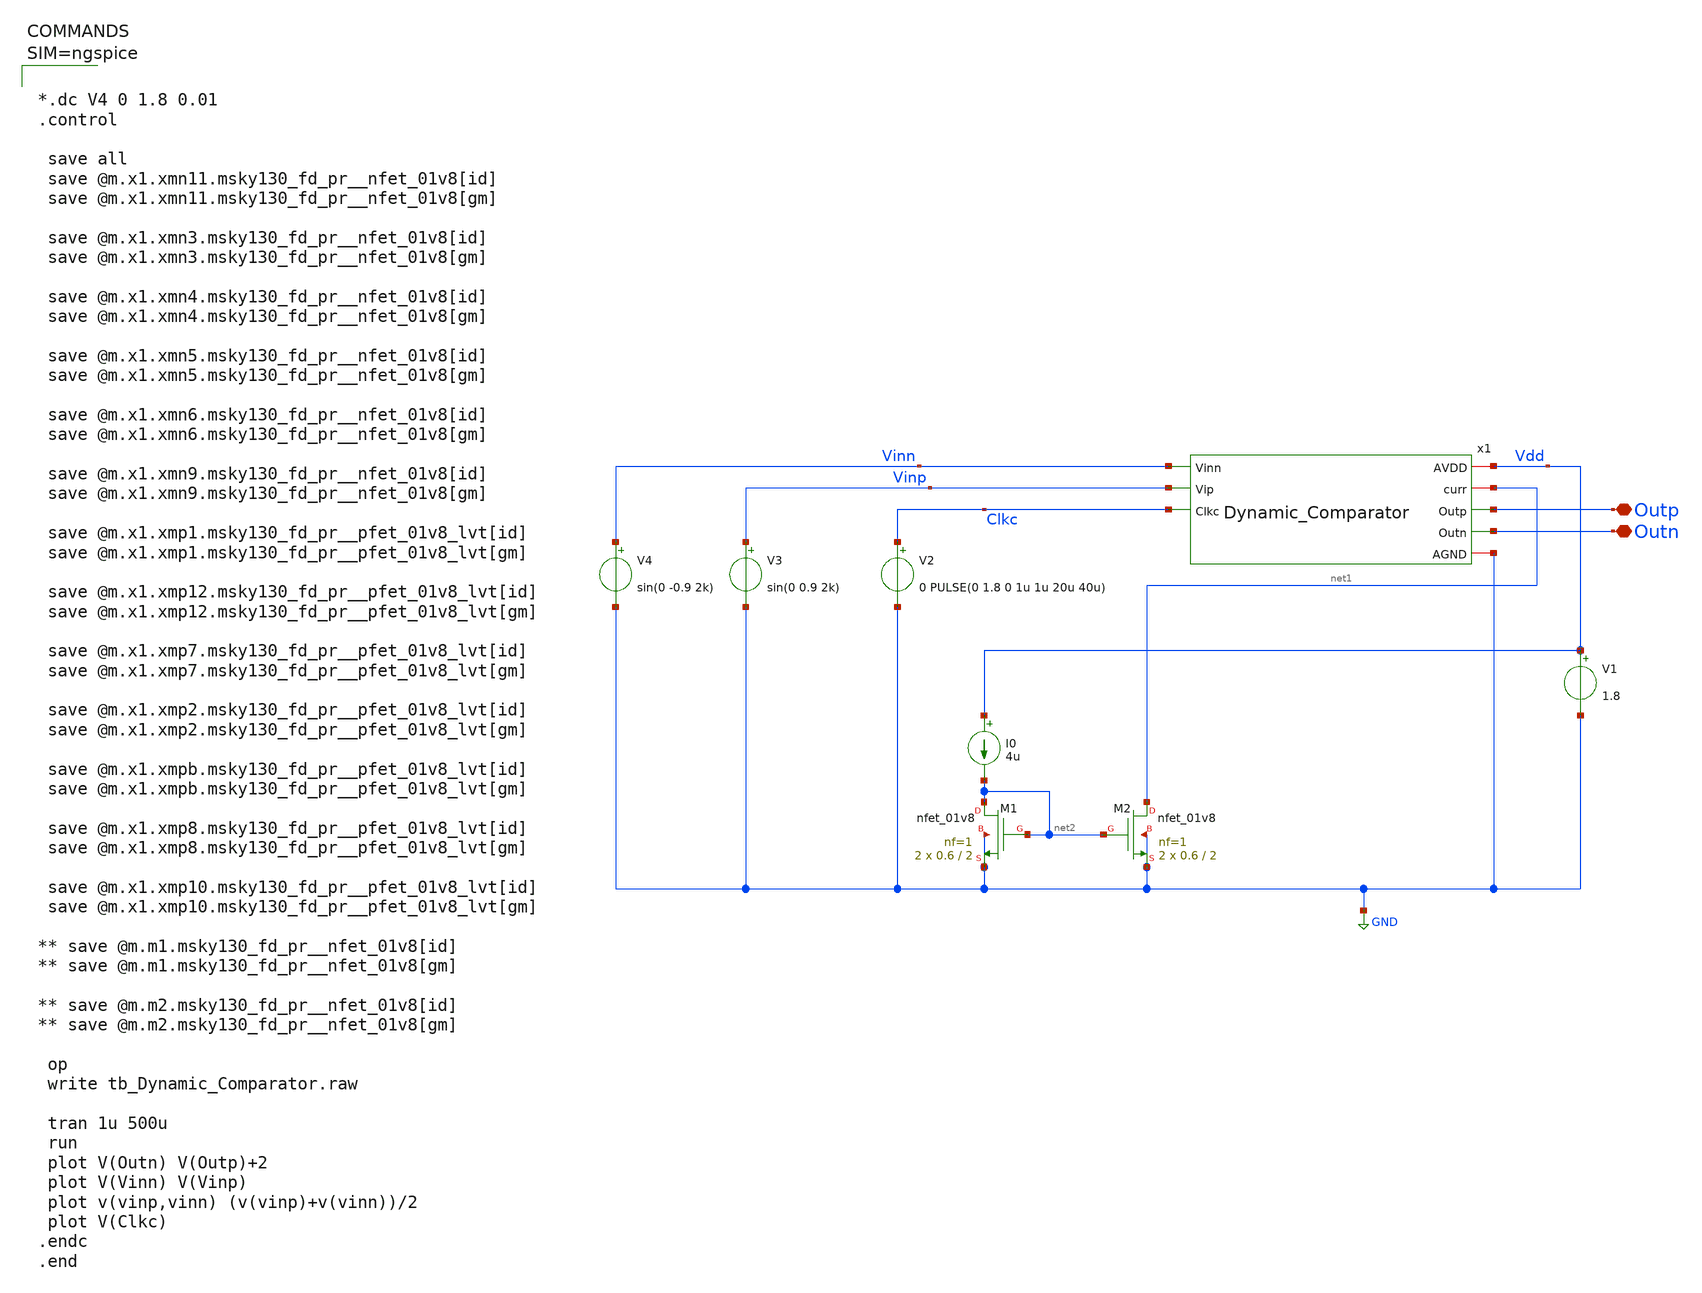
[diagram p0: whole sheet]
** sch_path: sar-adc/updated/tb_Dynamic_Comparator.sch
**.subckt tb_Dynamic_Comparator Outp Outn
*.iopin Outp
*.iopin Outn
V1 Vdd GND 1.8
V2 Clkc GND 0 PULSE(0 1.8 0 1u 1u 20u 40u)
V3 Vinp GND sin(0 0.9 2k)
V4 Vinn GND sin(0 -0.9 2k)
XM2 net1 net2 GND GND sky130_fd_pr__nfet_01v8 L=2 W=0.6 nf=1 ad='int((1 + 1)/2) * 0.6 / 1 * 0.29' as='int((1 + 2)/2) * 0.6 / 1 * 0.29'
+ pd='2*int((1 + 1)/2) * (0.6 / 1 + 0.29)' ps='2*int((1 + 2)/2) * (0.6 / 1 + 0.29)' nrd='0.29 / 0.6 ' nrs='0.29 / 0.6 '
+ sa=0 sb=0 sd=0 mult=2 m=2
XM1 net2 net2 GND GND sky130_fd_pr__nfet_01v8 L=2 W=0.6 nf=1 ad='int((1 + 1)/2) * 0.6 / 1 * 0.29' as='int((1 + 2)/2) * 0.6 / 1 * 0.29'
+ pd='2*int((1 + 1)/2) * (0.6 / 1 + 0.29)' ps='2*int((1 + 2)/2) * (0.6 / 1 + 0.29)' nrd='0.29 / 0.6 ' nrs='0.29 / 0.6 '
+ sa=0 sb=0 sd=0 mult=2 m=2
I0 Vdd net2 4u
x1 Vdd net1 Vinn Vinp Outp Outn Clkc GND Dynamic_Comparator
**** begin user architecture code

** opencircuitdesign pdks install
.lib $::SKYWATER_MODELS/sky130.lib.spice tt




*.dc V4 0 1.8 0.01
.control

 save all
 save @m.x1.xmn11.msky130_fd_pr__nfet_01v8[id]
 save @m.x1.xmn11.msky130_fd_pr__nfet_01v8[gm]

 save @m.x1.xmn3.msky130_fd_pr__nfet_01v8[id]
 save @m.x1.xmn3.msky130_fd_pr__nfet_01v8[gm]

 save @m.x1.xmn4.msky130_fd_pr__nfet_01v8[id]
 save @m.x1.xmn4.msky130_fd_pr__nfet_01v8[gm]

 save @m.x1.xmn5.msky130_fd_pr__nfet_01v8[id]
 save @m.x1.xmn5.msky130_fd_pr__nfet_01v8[gm]

 save @m.x1.xmn6.msky130_fd_pr__nfet_01v8[id]
 save @m.x1.xmn6.msky130_fd_pr__nfet_01v8[gm]

 save @m.x1.xmn9.msky130_fd_pr__nfet_01v8[id]
 save @m.x1.xmn9.msky130_fd_pr__nfet_01v8[gm]

 save @m.x1.xmp1.msky130_fd_pr__pfet_01v8_lvt[id]
 save @m.x1.xmp1.msky130_fd_pr__pfet_01v8_lvt[gm]

 save @m.x1.xmp12.msky130_fd_pr__pfet_01v8_lvt[id]
 save @m.x1.xmp12.msky130_fd_pr__pfet_01v8_lvt[gm]

 save @m.x1.xmp7.msky130_fd_pr__pfet_01v8_lvt[id]
 save @m.x1.xmp7.msky130_fd_pr__pfet_01v8_lvt[gm]

 save @m.x1.xmp2.msky130_fd_pr__pfet_01v8_lvt[id]
 save @m.x1.xmp2.msky130_fd_pr__pfet_01v8_lvt[gm]

 save @m.x1.xmpb.msky130_fd_pr__pfet_01v8_lvt[id]
 save @m.x1.xmpb.msky130_fd_pr__pfet_01v8_lvt[gm]

 save @m.x1.xmp8.msky130_fd_pr__pfet_01v8_lvt[id]
 save @m.x1.xmp8.msky130_fd_pr__pfet_01v8_lvt[gm]

 save @m.x1.xmp10.msky130_fd_pr__pfet_01v8_lvt[id]
 save @m.x1.xmp10.msky130_fd_pr__pfet_01v8_lvt[gm]

** save @m.m1.msky130_fd_pr__nfet_01v8[id]
** save @m.m1.msky130_fd_pr__nfet_01v8[gm]

** save @m.m2.msky130_fd_pr__nfet_01v8[id]
** save @m.m2.msky130_fd_pr__nfet_01v8[gm]

 op
 write tb_Dynamic_Comparator.raw

 tran 1u 500u
 run
 plot V(Outn) V(Outp)+2
 plot V(Vinn) V(Vinp)
 plot v(vinp,vinn) (v(vinp)+v(vinn))/2
 plot V(Clkc)
.endc
.end



**** end user architecture code
**.ends

* expanding   symbol:  Dynamic_Comparator.sym # of pins=8
** sym_path: sar-adc/updated/Dynamic_Comparator.sym
** sch_path: sar-adc/updated/Dynamic_Comparator.sch
.subckt Dynamic_Comparator AVDD curr Vinn Vip Outp Outn Clkc AGND
*.ipin Vip
*.ipin Vinn
*.opin Outn
*.opin Outp
*.ipin Clkc
*.iopin AVDD
*.iopin AGND
*.iopin curr
XMPB net1 curr AVDD AVDD sky130_fd_pr__pfet_01v8_lvt L=2 W=1.12 nf=1 ad='int((1 + 1)/2) * 1.12 / 1 * 0.29'
+ as='int((1 + 2)/2) * 1.12 / 1 * 0.29' pd='2*int((1 + 1)/2) * (1.12 / 1 + 0.29)' ps='2*int((1 + 2)/2) * (1.12 / 1 + 0.29)'
+ nrd='0.29 / 1.12 ' nrs='0.29 / 1.12 ' sa=0 sb=0 sd=0 mult=4 m=4
XMP7 net2 Clkc net1 AVDD sky130_fd_pr__pfet_01v8_lvt L=2 W=1.12 nf=1 ad='int((1 + 1)/2) * 1.12 / 1 * 0.29'
+ as='int((1 + 2)/2) * 1.12 / 1 * 0.29' pd='2*int((1 + 1)/2) * (1.12 / 1 + 0.29)' ps='2*int((1 + 2)/2) * (1.12 / 1 + 0.29)'
+ nrd='0.29 / 1.12 ' nrs='0.29 / 1.12 ' sa=0 sb=0 sd=0 mult=4 m=4
XMP12 curr curr AVDD AVDD sky130_fd_pr__pfet_01v8_lvt L=2 W=1.12 nf=1 ad='int((1 + 1)/2) * 1.12 / 1 * 0.29'
+ as='int((1 + 2)/2) * 1.12 / 1 * 0.29' pd='2*int((1 + 1)/2) * (1.12 / 1 + 0.29)' ps='2*int((1 + 2)/2) * (1.12 / 1 + 0.29)'
+ nrd='0.29 / 1.12 ' nrs='0.29 / 1.12 ' sa=0 sb=0 sd=0 mult=4 m=4
XMP1 net4 Vip net2 AVDD sky130_fd_pr__pfet_01v8_lvt L=2 W=2 nf=1 ad='int((1 + 1)/2) * 2 / 1 * 0.29' as='int((1 + 2)/2) * 2 / 1 * 0.29'
+ pd='2*int((1 + 1)/2) * (2 / 1 + 0.29)' ps='2*int((1 + 2)/2) * (2 / 1 + 0.29)' nrd='0.29 / 2 ' nrs='0.29 / 2 '
+ sa=0 sb=0 sd=0 mult=9 m=9
XMP2 net3 Vinn net2 AVDD sky130_fd_pr__pfet_01v8_lvt L=2 W=2 nf=1 ad='int((1 + 1)/2) * 2 / 1 * 0.29'
+ as='int((1 + 2)/2) * 2 / 1 * 0.29' pd='2*int((1 + 1)/2) * (2 / 1 + 0.29)' ps='2*int((1 + 2)/2) * (2 / 1 + 0.29)'
+ nrd='0.29 / 2 ' nrs='0.29 / 2 ' sa=0 sb=0 sd=0 mult=9 m=9
XMP8 Outp net4 AVDD AVDD sky130_fd_pr__pfet_01v8_lvt L=2 W=1.12 nf=1 ad='int((1 + 1)/2) * 1.12 / 1 * 0.29'
+ as='int((1 + 2)/2) * 1.12 / 1 * 0.29' pd='2*int((1 + 1)/2) * (1.12 / 1 + 0.29)' ps='2*int((1 + 2)/2) * (1.12 / 1 + 0.29)'
+ nrd='0.29 / 1.12 ' nrs='0.29 / 1.12 ' sa=0 sb=0 sd=0 mult=4 m=4
XMP10 Outn net3 AVDD AVDD sky130_fd_pr__pfet_01v8_lvt L=2 W=1.12 nf=1 ad='int((1 + 1)/2) * 1.12 / 1 * 0.29'
+ as='int((1 + 2)/2) * 1.12 / 1 * 0.29' pd='2*int((1 + 1)/2) * (1.12 / 1 + 0.29)' ps='2*int((1 + 2)/2) * (1.12 / 1 + 0.29)'
+ nrd='0.29 / 1.12 ' nrs='0.29 / 1.12 ' sa=0 sb=0 sd=0 mult=4 m=4
XMN5 net4 Clkc AGND AGND sky130_fd_pr__nfet_01v8 L=2 W=0.65 nf=1 ad='int((1 + 1)/2) * 0.65 / 1 * 0.29'
+ as='int((1 + 2)/2) * 0.65 / 1 * 0.29' pd='2*int((1 + 1)/2) * (0.65 / 1 + 0.29)' ps='2*int((1 + 2)/2) * (0.65 / 1 + 0.29)'
+ nrd='0.29 / 0.65 ' nrs='0.29 / 0.65 ' sa=0 sb=0 sd=0 mult=2 m=2
XMN3 net4 net3 AGND AGND sky130_fd_pr__nfet_01v8 L=2 W=0.6 nf=1 ad='int((1 + 1)/2) * 0.6 / 1 * 0.29'
+ as='int((1 + 2)/2) * 0.6 / 1 * 0.29' pd='2*int((1 + 1)/2) * (0.6 / 1 + 0.29)' ps='2*int((1 + 2)/2) * (0.6 / 1 + 0.29)'
+ nrd='0.29 / 0.6 ' nrs='0.29 / 0.6 ' sa=0 sb=0 sd=0 mult=2 m=2
XMN4 net3 net4 AGND AGND sky130_fd_pr__nfet_01v8 L=2 W=0.6 nf=1 ad='int((1 + 1)/2) * 0.6 / 1 * 0.29'
+ as='int((1 + 2)/2) * 0.6 / 1 * 0.29' pd='2*int((1 + 1)/2) * (0.6 / 1 + 0.29)' ps='2*int((1 + 2)/2) * (0.6 / 1 + 0.29)'
+ nrd='0.29 / 0.6 ' nrs='0.29 / 0.6 ' sa=0 sb=0 sd=0 mult=2 m=2
XMN6 net3 Clkc AGND AGND sky130_fd_pr__nfet_01v8 L=2 W=0.65 nf=1 ad='int((1 + 1)/2) * 0.65 / 1 * 0.29'
+ as='int((1 + 2)/2) * 0.65 / 1 * 0.29' pd='2*int((1 + 1)/2) * (0.65 / 1 + 0.29)' ps='2*int((1 + 2)/2) * (0.65 / 1 + 0.29)'
+ nrd='0.29 / 0.65 ' nrs='0.29 / 0.65 ' sa=0 sb=0 sd=0 mult=2 m=2
XMN9 Outp net4 AGND AGND sky130_fd_pr__nfet_01v8 L=2 W=0.6 nf=1 ad='int((1 + 1)/2) * 0.6 / 1 * 0.29'
+ as='int((1 + 2)/2) * 0.6 / 1 * 0.29' pd='2*int((1 + 1)/2) * (0.6 / 1 + 0.29)' ps='2*int((1 + 2)/2) * (0.6 / 1 + 0.29)'
+ nrd='0.29 / 0.6 ' nrs='0.29 / 0.6 ' sa=0 sb=0 sd=0 mult=2 m=2
XMN11 Outn net3 AGND AGND sky130_fd_pr__nfet_01v8 L=2 W=0.6 nf=1 ad='int((1 + 1)/2) * 0.6 / 1 * 0.29'
+ as='int((1 + 2)/2) * 0.6 / 1 * 0.29' pd='2*int((1 + 1)/2) * (0.6 / 1 + 0.29)' ps='2*int((1 + 2)/2) * (0.6 / 1 + 0.29)'
+ nrd='0.29 / 0.6 ' nrs='0.29 / 0.6 ' sa=0 sb=0 sd=0 mult=2 m=2
.ends

.GLOBAL GND
.end
